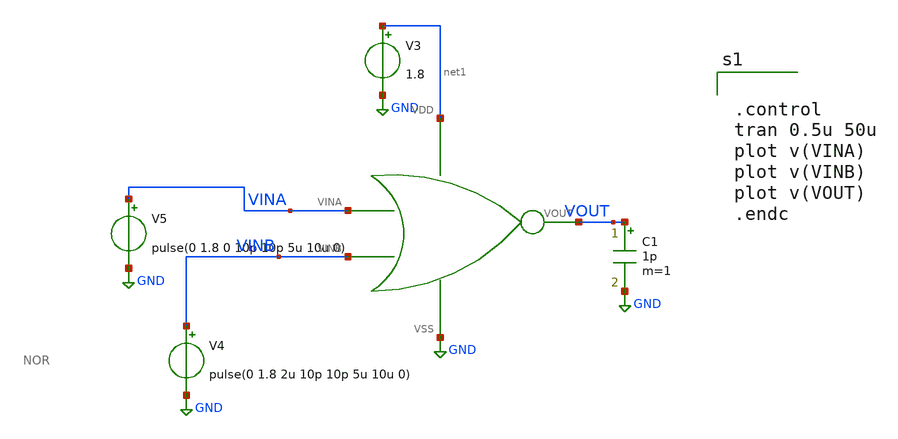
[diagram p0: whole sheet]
** sch_path: xschem/DC_DC_Converter_xschem/OTHERS/DC_DC_Converter_6/revised_delay-block/NOR_TB.sch
**.subckt NOR_TB
V3 net1 GND 1.8
V5 VINA GND pulse(0 1.8 0 10p 10p 5u 10u 0)
V4 VINB GND pulse(0 1.8 2u 10p 10p 5u 10u 0)
C1 VOUT GND 1p m=1
X1 VOUT VINA net1 GND VINB NOR
**** begin user architecture code


.control
tran 0.5u 50u
plot v(VINA)
plot v(VINB)
plot v(VOUT)
.endc



** opencircuitdesign pdks install
.lib $::SKYWATER_MODELS/sky130.lib.spice tt


**** end user architecture code
**.ends

* expanding   symbol:  NOR.sym # of pins=5
** sym_path: xschem/DC_DC_Converter_xschem/OTHERS/DC_DC_Converter_6/Delay_block_revised/NOR.sym
** sch_path: xschem/DC_DC_Converter_xschem/OTHERS/DC_DC_Converter_6/Delay_block_revised/NOR.sch
.subckt NOR VOUT VINA VDD VSS VINB
*.iopin VDD
*.iopin VSS
*.iopin VINB
*.iopin VINA
*.iopin VOUT
XM1 VOUT VINB VSS VSS sky130_fd_pr__nfet_01v8 L=0.15 W=200 nf=10 ad='int((nf+1)/2) * W/nf * 0.29' as='int((nf+2)/2) * W/nf * 0.29'
+ pd='2*int((nf+1)/2) * (W/nf + 0.29)' ps='2*int((nf+2)/2) * (W/nf + 0.29)' nrd='0.29 / W' nrs='0.29 / W'
+ sa=0 sb=0 sd=0 mult=1 m=1
XM2 VOUT VINB net1 VDD sky130_fd_pr__pfet_01v8 L=0.15 W=600 nf=20 ad='int((nf+1)/2) * W/nf * 0.29' as='int((nf+2)/2) * W/nf * 0.29'
+ pd='2*int((nf+1)/2) * (W/nf + 0.29)' ps='2*int((nf+2)/2) * (W/nf + 0.29)' nrd='0.29 / W' nrs='0.29 / W'
+ sa=0 sb=0 sd=0 mult=1 m=1
XM3 net1 VINA VDD VDD sky130_fd_pr__pfet_01v8 L=0.15 W=600 nf=20 ad='int((nf+1)/2) * W/nf * 0.29' as='int((nf+2)/2) * W/nf * 0.29'
+ pd='2*int((nf+1)/2) * (W/nf + 0.29)' ps='2*int((nf+2)/2) * (W/nf + 0.29)' nrd='0.29 / W' nrs='0.29 / W'
+ sa=0 sb=0 sd=0 mult=1 m=1
XM4 VOUT VINA VSS VSS sky130_fd_pr__nfet_01v8 L=0.15 W=200 nf=10 ad='int((nf+1)/2) * W/nf * 0.29' as='int((nf+2)/2) * W/nf * 0.29'
+ pd='2*int((nf+1)/2) * (W/nf + 0.29)' ps='2*int((nf+2)/2) * (W/nf + 0.29)' nrd='0.29 / W' nrs='0.29 / W'
+ sa=0 sb=0 sd=0 mult=1 m=1
.ends

.GLOBAL GND
.end
